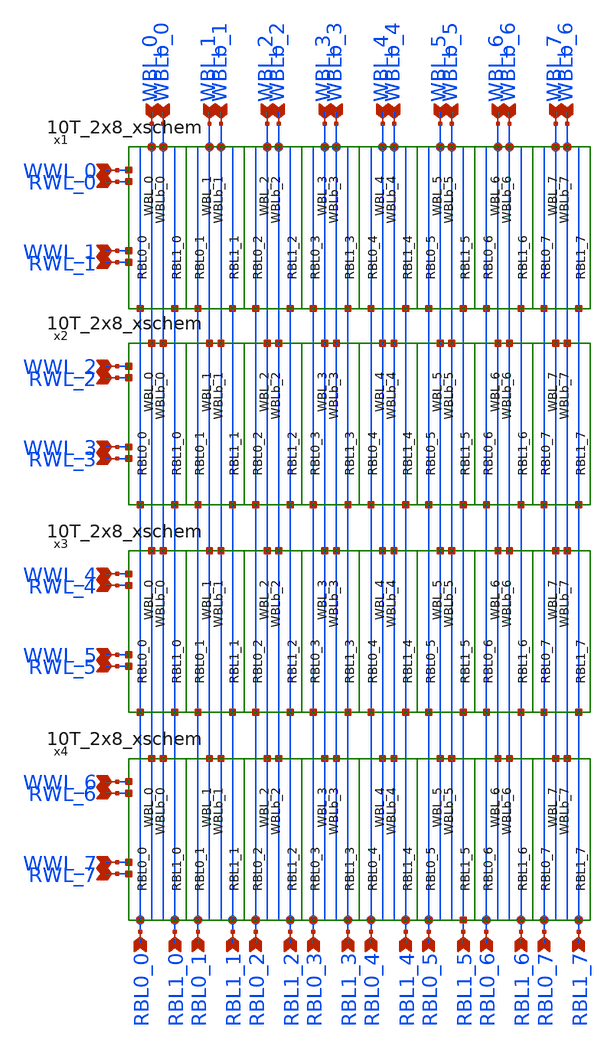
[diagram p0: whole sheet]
** sch_path: custom/xschem/10T_8x8_xschem.sch
**.subckt 10T_8x8_xschem WWL_0 WWL_1 RWL_1 RWL_0 WWL_2 RWL_2 WWL_3 RWL_3 WWL_4 RWL_4 WWL_5 RWL_5
*+ WWL_6 RWL_6 WWL_7 RWL_7 RBL0_0 RBL1_0 RBL0_1 RBL1_1 RBL0_2 RBL1_2 RBL0_3 RBL1_3 RBL0_4 RBL1_4 RBL0_5
*+ RBL1_5 RBL0_6 RBL1_6 RBL0_7 RBL1_7 WBL_0 WBLb_0 WBL_1 WBLb_1 WBL_2 WBLb_2 WBL_3 WBLb_3 WBL_4 WBLb_4 WBL_5
*+ WBLb_5 WBL_6 WBLb_6 WBL_7 WBLb_6
*.ipin WWL_0
*.ipin WWL_1
*.ipin RWL_1
*.ipin RWL_0
*.ipin WWL_2
*.ipin RWL_2
*.ipin WWL_3
*.ipin RWL_3
*.ipin WWL_4
*.ipin RWL_4
*.ipin WWL_5
*.ipin RWL_5
*.ipin WWL_6
*.ipin RWL_6
*.ipin WWL_7
*.ipin RWL_7
*.ipin RBL0_0
*.ipin RBL1_0
*.ipin RBL0_1
*.ipin RBL1_1
*.ipin RBL0_2
*.ipin RBL1_2
*.ipin RBL0_3
*.ipin RBL1_3
*.ipin RBL0_4
*.ipin RBL1_4
*.ipin RBL0_5
*.ipin RBL1_5
*.ipin RBL0_6
*.ipin RBL1_6
*.ipin RBL0_7
*.ipin RBL1_7
*.ipin WBL_0
*.ipin WBLb_0
*.ipin WBL_1
*.ipin WBLb_1
*.ipin WBL_2
*.ipin WBLb_2
*.ipin WBL_3
*.ipin WBLb_3
*.ipin WBL_4
*.ipin WBLb_4
*.ipin WBL_5
*.ipin WBLb_5
*.ipin WBL_6
*.ipin WBLb_6
*.ipin WBL_7
*.ipin WBLb_6
x1 WBLb_6 WBL_3 WBL_7 WBLb_6 WBLb_3 WBL_6 WBLb_2 WBL_4 WBL_0 WBLb_5 WBLb_0 WBLb_1 WBL_5 WBLb_4 WBL_2
+ WBL_1 WWL_0 RWL_0 WWL_1 RWL_1 RBL1_4 RBL1_3 RBL0_3 RBL1_2 RBL0_5 RBL1_0 RBL1_1 RBL0_6 RBL1_7 RBL0_2
+ RBL1_6 RBL0_7 RBL1_5 RBL0_1 RBL0_4 RBL0_0 10T_2x8_xschem
x2 WBLb_6 WBL_3 WBL_7 WBLb_6 WBLb_3 WBL_6 WBLb_2 WBL_4 WBL_0 WBLb_5 WBLb_0 WBLb_1 WBL_5 WBLb_4 WBL_2
+ WBL_1 WWL_2 RWL_2 WWL_3 RWL_3 RBL1_4 RBL1_3 RBL0_3 RBL1_2 RBL0_5 RBL1_0 RBL1_1 RBL0_6 RBL1_7 RBL0_2
+ RBL1_6 RBL0_7 RBL1_5 RBL0_1 RBL0_4 RBL0_0 10T_2x8_xschem
x3 WBLb_6 WBL_3 WBL_7 WBLb_6 WBLb_3 WBL_6 WBLb_2 WBL_4 WBL_0 WBLb_5 WBLb_0 WBLb_1 WBL_5 WBLb_4 WBL_2
+ WBL_1 WWL_4 RWL_4 WWL_5 RWL_5 RBL1_4 RBL1_3 RBL0_3 RBL1_2 RBL0_5 RBL1_0 RBL1_1 RBL0_6 RBL1_7 RBL0_2
+ RBL1_6 RBL0_7 RBL1_5 RBL0_1 RBL0_4 RBL0_0 10T_2x8_xschem
x4 WBLb_6 WBL_3 WBL_7 WBLb_6 WBLb_3 WBL_6 WBLb_2 WBL_4 WBL_0 WBLb_5 WBLb_0 WBLb_1 WBL_5 WBLb_4 WBL_2
+ WBL_1 WWL_6 RWL_6 WWL_7 RWL_7 RBL1_4 RBL1_3 RBL0_3 RBL1_2 RBL0_5 RBL1_0 RBL1_1 RBL0_6 RBL1_7 RBL0_2
+ RBL1_6 RBL0_7 RBL1_5 RBL0_1 RBL0_4 RBL0_0 10T_2x8_xschem
**.ends

* expanding   symbol:  10T_2x8_xschem.sym # of pins=36
** sym_path: custom/xschem/10T_2x8_xschem.sym
** sch_path: custom/xschem/10T_2x8_xschem.sch
.subckt 10T_2x8_xschem WBLb_6 WBL_3 WBL_7 WBLb_7 WBLb_3 WBL_6 WBLb_2 WBL_4 WBL_0 WBLb_5 WBLb_0
+ WBLb_1 WBL_5 WBLb_4 WBL_2 WBL_1 WWL_0 RWL_0 WWL_1 RWL_1 RBL1_4 RBL1_3 RBL0_3 RBL1_2 RBL0_5 RBL1_0 RBL1_1
+ RBL0_6 RBL1_7 RBL0_2 RBL1_6 RBL0_7 RBL1_5 RBL0_1 RBL0_4 RBL0_0
*.ipin WWL_0
*.ipin RWL_0
*.ipin WWL_1
*.ipin RWL_1
*.ipin RBL0_0
*.ipin RBL1_0
*.ipin RBL0_3
*.ipin RBL0_4
*.ipin RBL0_1
*.ipin RBL1_7
*.ipin RBL1_1
*.ipin RBL0_5
*.ipin RBL1_2
*.ipin RBL1_3
*.ipin RBL1_4
*.ipin RBL1_5
*.ipin RBL0_7
*.ipin RBL1_6
*.ipin RBL0_2
*.ipin RBL0_6
*.ipin WBLb_7
*.ipin WBLb_3
*.ipin WBL_6
*.ipin WBLb_4
*.ipin WBL_5
*.ipin WBLb_0
*.ipin WBLb_1
*.ipin WBLb_2
*.ipin WBL_0
*.ipin WBLb_5
*.ipin WBL_7
*.ipin WBL_4
*.ipin WBLb_6
*.ipin WBL_3
*.ipin WBL_2
*.ipin WBL_1
x1 WBL_1 WBL_2 WBL_3 WBLb_6 WBL_4 WBL_7 WBLb_5 WBL_0 WBLb_2 WBLb_1 WBLb_0 WBL_5 WBLb_4 WBL_6 WBLb_3
+ WBLb_7 WWL_0 RWL_0 RBL0_6 RBL0_2 RBL1_6 RBL0_7 RBL1_5 RBL1_4 RBL1_3 RBL1_2 RBL0_5 RBL1_1 RBL1_7 RBL0_1
+ RBL0_4 RBL0_3 RBL1_0 RBL0_0 VDD GND 10T_1x8_xschem
x2 WBL_1 WBL_2 WBL_3 WBLb_6 WBL_4 WBL_7 WBLb_5 WBL_0 WBLb_2 WBLb_1 WBLb_0 WBL_5 WBLb_4 WBL_6 WBLb_3
+ WBLb_7 WWL_1 RWL_1 RBL0_6 RBL0_2 RBL1_6 RBL0_7 RBL1_5 RBL1_4 RBL1_3 RBL1_2 RBL0_5 RBL1_1 RBL1_7 RBL0_1
+ RBL0_4 RBL0_3 RBL1_0 RBL0_0 VDD GND 10T_1x8_xschem
.ends


* expanding   symbol:  10T_1x8_xschem.sym # of pins=34
** sym_path: custom/xschem/10T_1x8_xschem.sym
** sch_path: custom/xschem/10T_1x8_xschem.sch
.subckt 10T_1x8_xschem WBL_1 WBL_2 WBL_3 WBLb_6 WBL_4 WBL_7 WBLb_5 WBL_0 WBLb_2 WBLb_1 WBLb_0 WBL_5
+ WBLb_4 WBL_6 WBLb_3 WBLb_7 WWL RWL RBL0_6 RBL0_2 RBL1_6 RBL0_7 RBL1_5 RBL1_4 RBL1_3 RBL1_2 RBL0_5 RBL1_1
+ RBL1_7 RBL0_1 RBL0_4 RBL0_3 RBL1_0 RBL0_0 VDD GND
*.ipin WBLb_0
*.opin RBL0_0
*.ipin WBL_0
*.ipin WBLb_1
*.ipin WBL_1
*.ipin WBLb_2
*.ipin WBL_2
*.ipin WBLb_3
*.ipin WBL_3
*.ipin WBLb_4
*.ipin WBL_4
*.ipin WBL_5
*.ipin WBLb_5
*.ipin WBL_6
*.ipin WBLb_6
*.ipin WBLb_7
*.ipin WBL_7
*.opin RBL1_0
*.opin RBL0_1
*.opin RBL1_1
*.opin RBL0_2
*.opin RBL1_2
*.opin RBL0_3
*.opin RBL1_3
*.opin RBL0_4
*.opin RBL1_4
*.opin RBL0_5
*.opin RBL1_5
*.opin RBL0_6
*.opin RBL1_6
*.opin RBL0_7
*.opin RBL1_7
*.ipin WWL
*.ipin RWL
x1 WWL WBL_0 RBL0_0 RBL1_0 WBLb_0 RWL RWL VDD GND 10T_toy_xschem
x2 WWL WBL_1 RBL0_1 RBL1_1 WBLb_1 RWL RWL VDD GND 10T_toy_xschem
x3 WWL WBL_2 RBL0_2 RBL1_2 WBLb_2 RWL RWL VDD GND 10T_toy_xschem
x4 WWL WBL_3 RBL0_3 RBL1_3 WBLb_3 RWL RWL VDD GND 10T_toy_xschem
x5 WWL WBL_4 RBL0_4 RBL1_4 WBLb_4 RWL RWL VDD GND 10T_toy_xschem
x6 WWL WBL_5 RBL0_5 RBL1_5 WBLb_5 RWL RWL VDD GND 10T_toy_xschem
x7 WWL WBL_6 RBL0_6 RBL1_6 WBLb_6 RWL RWL VDD GND 10T_toy_xschem
x8 WWL WBL_7 RBL0_7 RBL1_7 WBLb_7 RWL RWL VDD GND 10T_toy_xschem
.ends


* expanding   symbol:  10T_toy_xschem.sym # of pins=7
** sym_path: custom/xschem/10T_toy_xschem.sym
** sch_path: custom/xschem/10T_toy_xschem.sch
.subckt 10T_toy_xschem WWL WBL RBL0 RBL1 WBLb RWL0 RWL1 VDD GND
*.ipin WWL
*.ipin RWL0
*.ipin RWL1
*.ipin WBL
*.ipin WBLb
*.opin RBL0
*.opin RBL1
x1 net1 net2 VDD GND INVX1
x2 net2 net1 VDD GND INVX1
XM1 net2 WWL WBL GND sky130_fd_pr__nfet_01v8 L=0.15 W=0.14 nf=1 ad='int((nf+1)/2) * W/nf * 0.29' as='int((nf+2)/2) * W/nf * 0.29'
+ pd='2*int((nf+1)/2) * (W/nf + 0.29)' ps='2*int((nf+2)/2) * (W/nf + 0.29)' nrd='0.29 / W' nrs='0.29 / W'
+ sa=0 sb=0 sd=0 mult=1 m=1
XM2 WBLb WWL net1 GND sky130_fd_pr__nfet_01v8 L=0.15 W=0.14 nf=1 ad='int((nf+1)/2) * W/nf * 0.29' as='int((nf+2)/2) * W/nf * 0.29'
+ pd='2*int((nf+1)/2) * (W/nf + 0.29)' ps='2*int((nf+2)/2) * (W/nf + 0.29)' nrd='0.29 / W' nrs='0.29 / W'
+ sa=0 sb=0 sd=0 mult=1 m=1
XM3 net3 net2 GND GND sky130_fd_pr__nfet_01v8 L=0.15 W=0.14 nf=1 ad='int((nf+1)/2) * W/nf * 0.29' as='int((nf+2)/2) * W/nf * 0.29'
+ pd='2*int((nf+1)/2) * (W/nf + 0.29)' ps='2*int((nf+2)/2) * (W/nf + 0.29)' nrd='0.29 / W' nrs='0.29 / W'
+ sa=0 sb=0 sd=0 mult=1 m=1
XM4 RBL0 RWL0 net3 GND sky130_fd_pr__nfet_01v8 L=0.15 W=0.21 nf=1 ad='int((nf+1)/2) * W/nf * 0.29' as='int((nf+2)/2) * W/nf * 0.29'
+ pd='2*int((nf+1)/2) * (W/nf + 0.29)' ps='2*int((nf+2)/2) * (W/nf + 0.29)' nrd='0.29 / W' nrs='0.29 / W'
+ sa=0 sb=0 sd=0 mult=1 m=1
XM5 net4 net1 GND GND sky130_fd_pr__nfet_01v8 L=0.15 W=0.14 nf=1 ad='int((nf+1)/2) * W/nf * 0.29' as='int((nf+2)/2) * W/nf * 0.29'
+ pd='2*int((nf+1)/2) * (W/nf + 0.29)' ps='2*int((nf+2)/2) * (W/nf + 0.29)' nrd='0.29 / W' nrs='0.29 / W'
+ sa=0 sb=0 sd=0 mult=1 m=1
XM6 RBL1 RWL1 net4 GND sky130_fd_pr__nfet_01v8 L=0.15 W=0.21 nf=1 ad='int((nf+1)/2) * W/nf * 0.29' as='int((nf+2)/2) * W/nf * 0.29'
+ pd='2*int((nf+1)/2) * (W/nf + 0.29)' ps='2*int((nf+2)/2) * (W/nf + 0.29)' nrd='0.29 / W' nrs='0.29 / W'
+ sa=0 sb=0 sd=0 mult=1 m=1
.ends


* expanding   symbol:  INVX1.sym # of pins=2
** sym_path: custom/xschem/INVX1.sym
** sch_path: custom/xschem/INVX1.sch
.subckt INVX1 Y A VDD GND
*.ipin A
*.opin Y
XM1 Y A GND GND sky130_fd_pr__nfet_01v8 L=0.15 W=0.21 nf=1 ad='int((nf+1)/2) * W/nf * 0.29' as='int((nf+2)/2) * W/nf * 0.29'
+ pd='2*int((nf+1)/2) * (W/nf + 0.29)' ps='2*int((nf+2)/2) * (W/nf + 0.29)' nrd='0.29 / W' nrs='0.29 / W'
+ sa=0 sb=0 sd=0 mult=1 m=1
XM2 Y A VDD VDD sky130_fd_pr__pfet_01v8 L=0.15 W=0.14 nf=1 ad='int((nf+1)/2) * W/nf * 0.29' as='int((nf+2)/2) * W/nf * 0.29'
+ pd='2*int((nf+1)/2) * (W/nf + 0.29)' ps='2*int((nf+2)/2) * (W/nf + 0.29)' nrd='0.29 / W' nrs='0.29 / W'
+ sa=0 sb=0 sd=0 mult=1 m=1
.ends

.end
